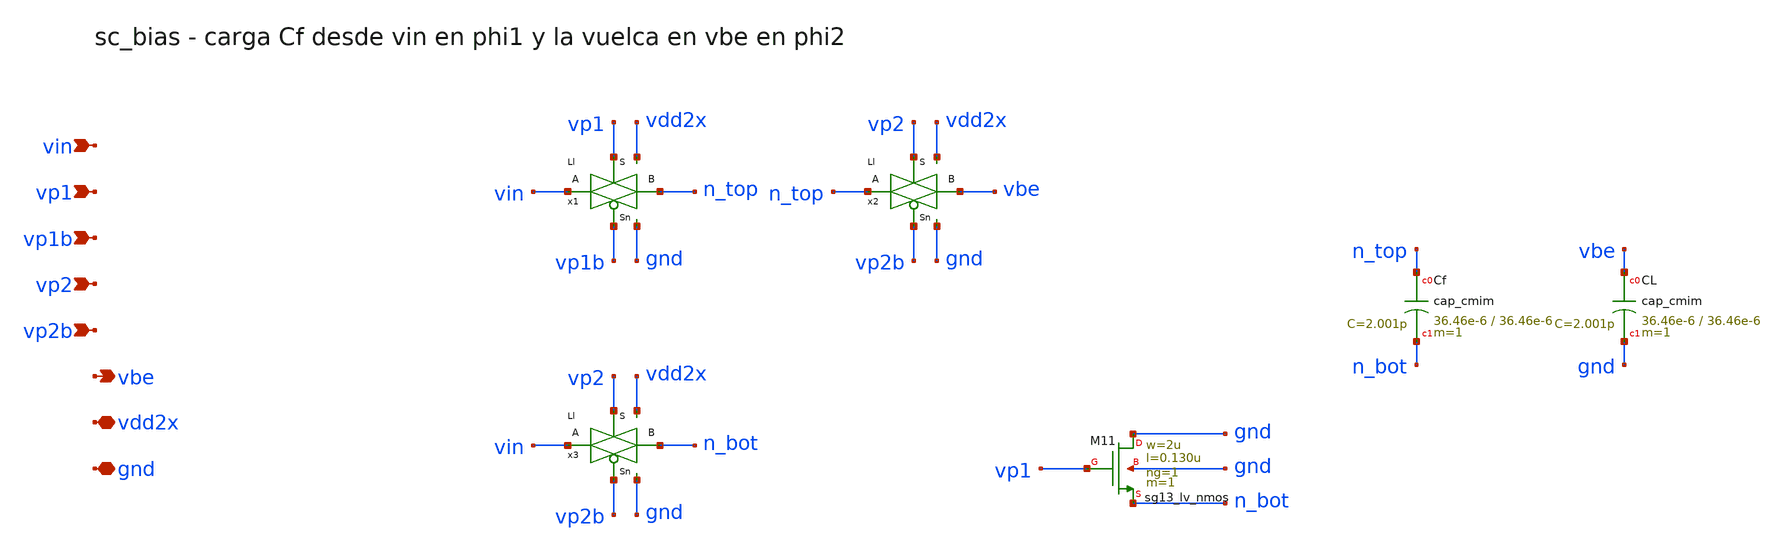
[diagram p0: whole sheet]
** sch_path: Enfoque_A/xschem/celdas/sc_bias.sch
**.subckt sc_bias vin vp1 vp1b vp2 vp2b vbe vdd2x gnd
*.ipin vin
*.ipin vp1
*.ipin vp1b
*.ipin vp2
*.ipin vp2b
*.opin vbe
*.iopin vdd2x
*.iopin gnd
x1 vin n_top vp1 vp1b vdd2x gnd Ll
x2 n_top vbe vp2 vp2b vdd2x gnd Ll
x3 vin n_bot vp2 vp2b vdd2x gnd Ll
XM11 gnd vp1 n_bot gnd sg13_lv_nmos w=2u l=0.130u ng=1 m=1 mm_ok=1
XCf n_top n_bot cap_cmim w=36.46e-6 l=36.46e-6 m=1 mm_ok=1
XCL vbe gnd cap_cmim w=36.46e-6 l=36.46e-6 m=1 mm_ok=1
**.ends

* expanding   symbol:  Enfoque_A/xschem/celdas/Ll.sym # of pins=6
** sym_path: Enfoque_A/xschem/celdas/Ll.sym
** sch_path: Enfoque_A/xschem/celdas/Ll.sch
.subckt Ll A B S Sn vdd gnd
*.iopin gnd
*.iopin vdd
*.iopin B
*.ipin Sn
*.ipin S
*.iopin A
XM101 A S B gnd sg13_lv_nmos w=0.13u l=0.130u ng=1 m=1 mm_ok=1
XM100 B Sn A vdd sg13_lv_pmos w=0.3u l=0.130u ng=1 m=1 mm_ok=1
.ends

.end
